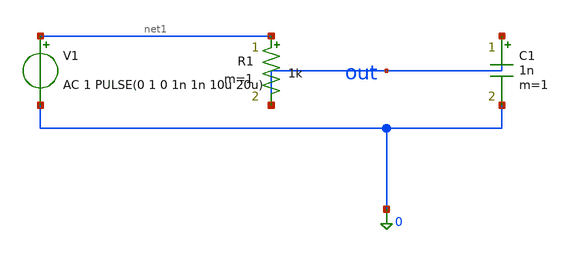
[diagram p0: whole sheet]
** sch_path: rc_lowpass.sch
**.subckt rc_lowpass
V1 net1 0 AC 1 PULSE(0 1 0 1n 1n 10u 20u)
R1 net1 out 1k m=1
C1 out 0 1n m=1
**** begin user architecture code


.ac dec 50 100 100meg




.tran 100n 25u uic


**** end user architecture code
**.ends
.end
